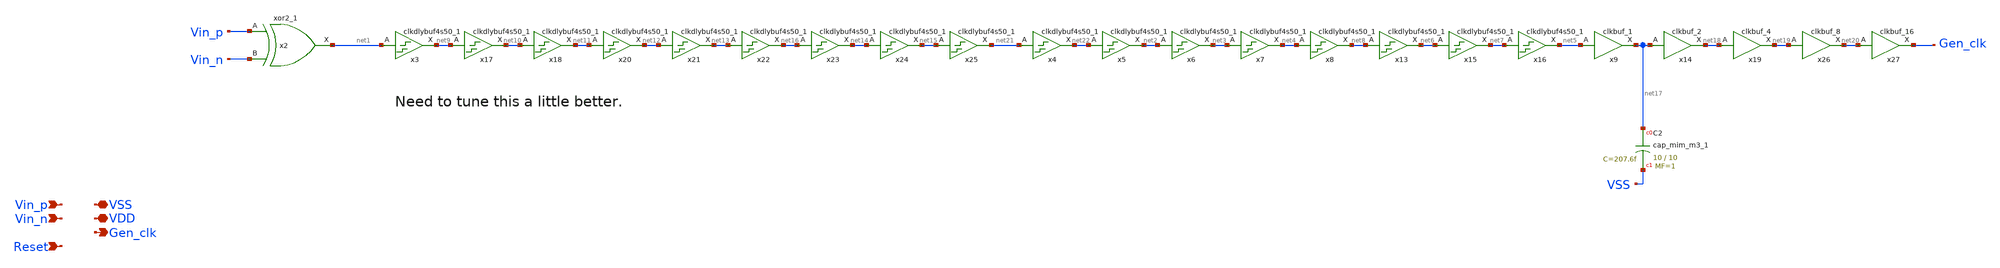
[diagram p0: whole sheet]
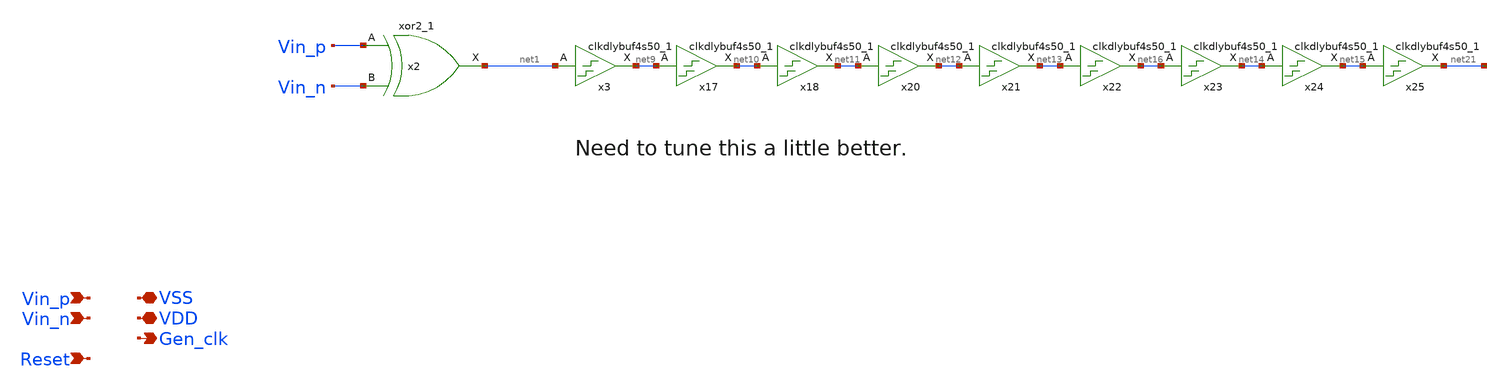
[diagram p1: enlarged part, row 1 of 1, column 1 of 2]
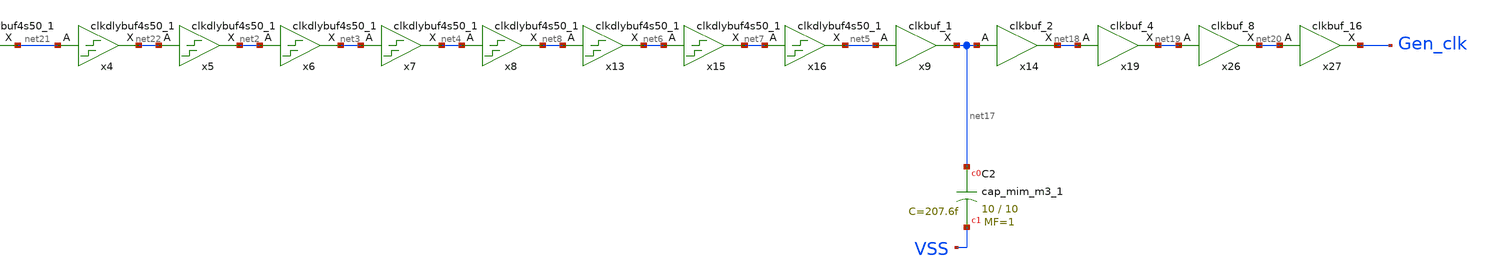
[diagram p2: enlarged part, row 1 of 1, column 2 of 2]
** sch_path: xschem/src/xor_clock_gen/xor_clock_gen.sch
**.subckt xor_clock_gen Vin_p VSS Gen_clk VDD Vin_n Reset
*.ipin Vin_p
*.iopin VSS
*.opin Gen_clk
*.iopin VDD
*.ipin Vin_n
*.ipin Reset
x2 Vin_p Vin_n VSS VSS VDD VDD net1 sky130_fd_sc_hd__xor2_1
x3 net1 VSS VSS VDD VDD net9 sky130_fd_sc_hd__clkdlybuf4s50_1
x4 net21 VSS VSS VDD VDD net22 sky130_fd_sc_hd__clkdlybuf4s50_1
x5 net22 VSS VSS VDD VDD net2 sky130_fd_sc_hd__clkdlybuf4s50_1
x6 net2 VSS VSS VDD VDD net3 sky130_fd_sc_hd__clkdlybuf4s50_1
x7 net3 VSS VSS VDD VDD net4 sky130_fd_sc_hd__clkdlybuf4s50_1
x8 net4 VSS VSS VDD VDD net8 sky130_fd_sc_hd__clkdlybuf4s50_1
x13 net8 VSS VSS VDD VDD net6 sky130_fd_sc_hd__clkdlybuf4s50_1
x15 net6 VSS VSS VDD VDD net7 sky130_fd_sc_hd__clkdlybuf4s50_1
x16 net7 VSS VSS VDD VDD net5 sky130_fd_sc_hd__clkdlybuf4s50_1
x17 net9 VSS VSS VDD VDD net10 sky130_fd_sc_hd__clkdlybuf4s50_1
x18 net10 VSS VSS VDD VDD net11 sky130_fd_sc_hd__clkdlybuf4s50_1
x20 net11 VSS VSS VDD VDD net12 sky130_fd_sc_hd__clkdlybuf4s50_1
x21 net12 VSS VSS VDD VDD net13 sky130_fd_sc_hd__clkdlybuf4s50_1
x22 net13 VSS VSS VDD VDD net16 sky130_fd_sc_hd__clkdlybuf4s50_1
x23 net16 VSS VSS VDD VDD net14 sky130_fd_sc_hd__clkdlybuf4s50_1
x24 net14 VSS VSS VDD VDD net15 sky130_fd_sc_hd__clkdlybuf4s50_1
x25 net15 VSS VSS VDD VDD net21 sky130_fd_sc_hd__clkdlybuf4s50_1
x9 net5 VSS VSS VDD VDD net17 sky130_fd_sc_hd__clkbuf_1
x14 net17 VSS VSS VDD VDD net18 sky130_fd_sc_hd__clkbuf_2
x19 net18 VSS VSS VDD VDD net19 sky130_fd_sc_hd__clkbuf_4
x26 net19 VSS VSS VDD VDD net20 sky130_fd_sc_hd__clkbuf_8
x27 net20 VSS VSS VDD VDD Gen_clk sky130_fd_sc_hd__clkbuf_16
XC2 net17 VSS sky130_fd_pr__cap_mim_m3_1 W=10 L=10 MF=1 m=1
**.ends
.end
